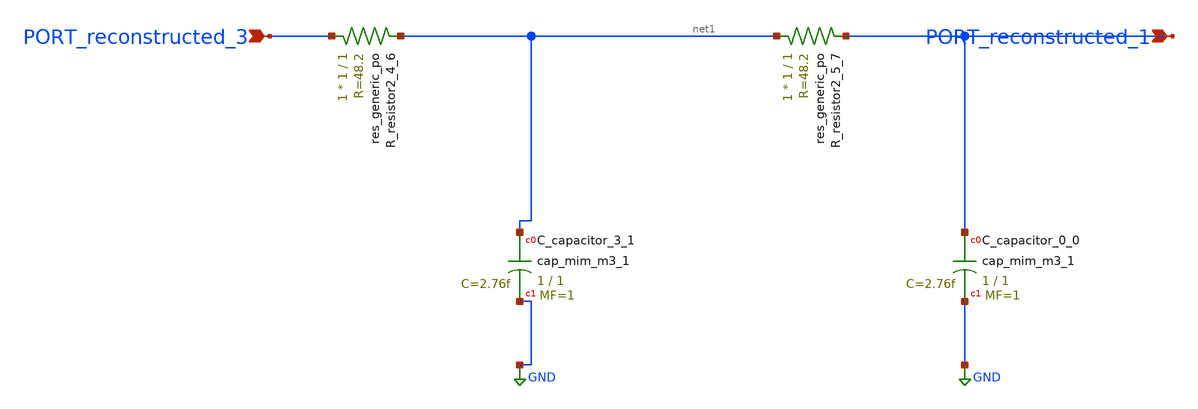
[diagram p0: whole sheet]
** sch_path: schematics/AMSNet/403.sch
**.subckt 403 PORT_reconstructed_1 PORT_reconstructed_3
*.ipin PORT_reconstructed_1
*.ipin PORT_reconstructed_3
XC_capacitor_0_0 PORT_reconstructed_1 GND sky130_fd_pr__cap_mim_m3_1 W=1 L=1 MF=1 m=1
XC_capacitor_3_1 net1 GND sky130_fd_pr__cap_mim_m3_1 W=1 L=1 MF=1 m=1
XR_resistor2_4_6 PORT_reconstructed_3 net1 sky130_fd_pr__res_generic_po W=1 L=1 m=1
XR_resistor2_5_7 net1 PORT_reconstructed_1 sky130_fd_pr__res_generic_po W=1 L=1 m=1
**.ends
.GLOBAL GND
.end
